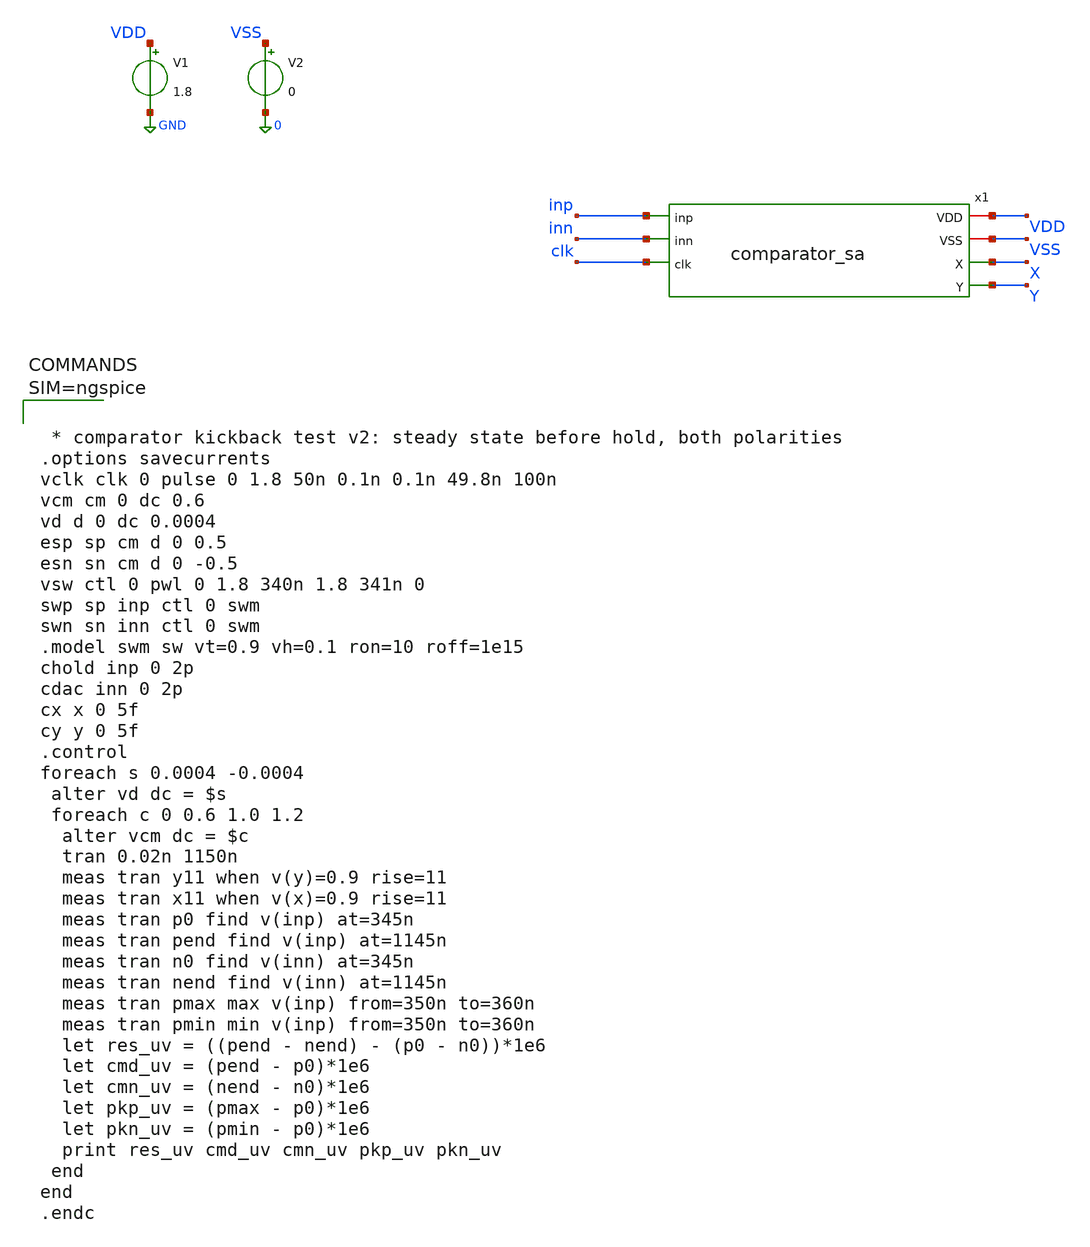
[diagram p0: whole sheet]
** sch_path: xschem/comparator_kick_tb.sch
**.subckt comparator_kick_tb
V1 VDD GND 1.8
V2 VSS 0 0
x1 inp VDD inn clk VSS X Y comparator_sa
**** begin user architecture code

** opencircuitdesign pdks install
.lib $::SKYWATER_MODELS/sky130.lib.spice tt




 * comparator kickback test v2: steady state before hold, both polarities
.options savecurrents
vclk clk 0 pulse 0 1.8 50n 0.1n 0.1n 49.8n 100n
vcm cm 0 dc 0.6
vd d 0 dc 0.0004
esp sp cm d 0 0.5
esn sn cm d 0 -0.5
vsw ctl 0 pwl 0 1.8 340n 1.8 341n 0
swp sp inp ctl 0 swm
swn sn inn ctl 0 swm
.model swm sw vt=0.9 vh=0.1 ron=10 roff=1e15
chold inp 0 2p
cdac inn 0 2p
cx x 0 5f
cy y 0 5f
.control
foreach s 0.0004 -0.0004
 alter vd dc = $s
 foreach c 0 0.6 1.0 1.2
  alter vcm dc = $c
  tran 0.02n 1150n
  meas tran y11 when v(y)=0.9 rise=11
  meas tran x11 when v(x)=0.9 rise=11
  meas tran p0 find v(inp) at=345n
  meas tran pend find v(inp) at=1145n
  meas tran n0 find v(inn) at=345n
  meas tran nend find v(inn) at=1145n
  meas tran pmax max v(inp) from=350n to=360n
  meas tran pmin min v(inp) from=350n to=360n
  let res_uv = ((pend - nend) - (p0 - n0))*1e6
  let cmd_uv = (pend - p0)*1e6
  let cmn_uv = (nend - n0)*1e6
  let pkp_uv = (pmax - p0)*1e6
  let pkn_uv = (pmin - p0)*1e6
  print res_uv cmd_uv cmn_uv pkp_uv pkn_uv
 end
end
.endc



**** end user architecture code
**.ends

* expanding   symbol:  comparator_sa.sym # of pins=7
** sym_path: xschem/comparator_sa.sym
** sch_path: xschem/comparator_sa.sch
.subckt comparator_sa inp VDD inn clk VSS X Y
*.ipin inp
*.ipin inn
*.ipin clk
*.opin X
*.opin Y
*.iopin VDD
*.iopin VSS
XM7 T ckb VDD VDD sky130_fd_pr__pfet_01v8 L=0.15 W=4 nf=1 ad='int((1 + 1)/2) * 4 / 1 * 0.29' as='int((1 + 2)/2) * 4 / 1 * 0.29'
+ pd='2*int((1 + 1)/2) * (4 / 1 + 0.29)' ps='2*int((1 + 2)/2) * (4 / 1 + 0.29)' nrd='0.29 / 4 ' nrs='0.29 / 4 '
+ sa=0 sb=0 sd=0 mult=1 m=1
XM1 P inp T T sky130_fd_pr__pfet_01v8 L=0.5 W=8 nf=4 ad='int((4 + 1)/2) * 8 / 4 * 0.29' as='int((4 + 2)/2) * 8 / 4 * 0.29'
+ pd='2*int((4 + 1)/2) * (8 / 4 + 0.29)' ps='2*int((4 + 2)/2) * (8 / 4 + 0.29)' nrd='0.29 / 8 ' nrs='0.29 / 8 '
+ sa=0 sb=0 sd=0 mult=1 m=1
XM2 Q inn T T sky130_fd_pr__pfet_01v8 L=0.5 W=8 nf=4 ad='int((4 + 1)/2) * 8 / 4 * 0.29' as='int((4 + 2)/2) * 8 / 4 * 0.29'
+ pd='2*int((4 + 1)/2) * (8 / 4 + 0.29)' ps='2*int((4 + 2)/2) * (8 / 4 + 0.29)' nrd='0.29 / 8 ' nrs='0.29 / 8 '
+ sa=0 sb=0 sd=0 mult=1 m=1
XM3 X Y P VDD sky130_fd_pr__pfet_01v8 L=0.15 W=2 nf=1 ad='int((1 + 1)/2) * 2 / 1 * 0.29' as='int((1 + 2)/2) * 2 / 1 * 0.29'
+ pd='2*int((1 + 1)/2) * (2 / 1 + 0.29)' ps='2*int((1 + 2)/2) * (2 / 1 + 0.29)' nrd='0.29 / 2 ' nrs='0.29 / 2 '
+ sa=0 sb=0 sd=0 mult=1 m=1
XM4 Y X Q VDD sky130_fd_pr__pfet_01v8 L=0.15 W=2 nf=1 ad='int((1 + 1)/2) * 2 / 1 * 0.29' as='int((1 + 2)/2) * 2 / 1 * 0.29'
+ pd='2*int((1 + 1)/2) * (2 / 1 + 0.29)' ps='2*int((1 + 2)/2) * (2 / 1 + 0.29)' nrd='0.29 / 2 ' nrs='0.29 / 2 '
+ sa=0 sb=0 sd=0 mult=1 m=1
XM6 Y X VSS VSS sky130_fd_pr__nfet_01v8 L=0.15 W=1 nf=1 ad='int((1 + 1)/2) * 1 / 1 * 0.29' as='int((1 + 2)/2) * 1 / 1 * 0.29'
+ pd='2*int((1 + 1)/2) * (1 / 1 + 0.29)' ps='2*int((1 + 2)/2) * (1 / 1 + 0.29)' nrd='0.29 / 1 ' nrs='0.29 / 1 '
+ sa=0 sb=0 sd=0 mult=1 m=1
XM5 X Y VSS VSS sky130_fd_pr__nfet_01v8 L=0.15 W=1 nf=1 ad='int((1 + 1)/2) * 1 / 1 * 0.29' as='int((1 + 2)/2) * 1 / 1 * 0.29'
+ pd='2*int((1 + 1)/2) * (1 / 1 + 0.29)' ps='2*int((1 + 2)/2) * (1 / 1 + 0.29)' nrd='0.29 / 1 ' nrs='0.29 / 1 '
+ sa=0 sb=0 sd=0 mult=1 m=1
XS4 Y ckb VSS VSS sky130_fd_pr__nfet_01v8 L=0.6 W=2 nf=1 ad='int((1 + 1)/2) * 2 / 1 * 0.29' as='int((1 + 2)/2) * 2 / 1 * 0.29'
+ pd='2*int((1 + 1)/2) * (2 / 1 + 0.29)' ps='2*int((1 + 2)/2) * (2 / 1 + 0.29)' nrd='0.29 / 2 ' nrs='0.29 / 2 '
+ sa=0 sb=0 sd=0 mult=1 m=1
XS2 Q ckb VSS VSS sky130_fd_pr__nfet_01v8 L=0.6 W=2 nf=1 ad='int((1 + 1)/2) * 2 / 1 * 0.29' as='int((1 + 2)/2) * 2 / 1 * 0.29'
+ pd='2*int((1 + 1)/2) * (2 / 1 + 0.29)' ps='2*int((1 + 2)/2) * (2 / 1 + 0.29)' nrd='0.29 / 2 ' nrs='0.29 / 2 '
+ sa=0 sb=0 sd=0 mult=1 m=1
XS3 X ckb VSS VSS sky130_fd_pr__nfet_01v8 L=0.6 W=2 nf=1 ad='int((1 + 1)/2) * 2 / 1 * 0.29' as='int((1 + 2)/2) * 2 / 1 * 0.29'
+ pd='2*int((1 + 1)/2) * (2 / 1 + 0.29)' ps='2*int((1 + 2)/2) * (2 / 1 + 0.29)' nrd='0.29 / 2 ' nrs='0.29 / 2 '
+ sa=0 sb=0 sd=0 mult=1 m=1
XS1 P ckb VSS VSS sky130_fd_pr__nfet_01v8 L=0.6 W=2 nf=1 ad='int((1 + 1)/2) * 2 / 1 * 0.29' as='int((1 + 2)/2) * 2 / 1 * 0.29'
+ pd='2*int((1 + 1)/2) * (2 / 1 + 0.29)' ps='2*int((1 + 2)/2) * (2 / 1 + 0.29)' nrd='0.29 / 2 ' nrs='0.29 / 2 '
+ sa=0 sb=0 sd=0 mult=1 m=1
XMIN ckb clk VSS VSS sky130_fd_pr__nfet_01v8 L=0.15 W=1 nf=1 ad='int((1 + 1)/2) * 1 / 1 * 0.29' as='int((1 + 2)/2) * 1 / 1 * 0.29'
+ pd='2*int((1 + 1)/2) * (1 / 1 + 0.29)' ps='2*int((1 + 2)/2) * (1 / 1 + 0.29)' nrd='0.29 / 1 ' nrs='0.29 / 1 '
+ sa=0 sb=0 sd=0 mult=1 m=1
XMIP ckb clk VDD VDD sky130_fd_pr__pfet_01v8 L=0.15 W=2 nf=1 ad='int((1 + 1)/2) * 2 / 1 * 0.29' as='int((1 + 2)/2) * 2 / 1 * 0.29'
+ pd='2*int((1 + 1)/2) * (2 / 1 + 0.29)' ps='2*int((1 + 2)/2) * (2 / 1 + 0.29)' nrd='0.29 / 2 ' nrs='0.29 / 2 '
+ sa=0 sb=0 sd=0 mult=1 m=1
.ends

.GLOBAL GND
.end
